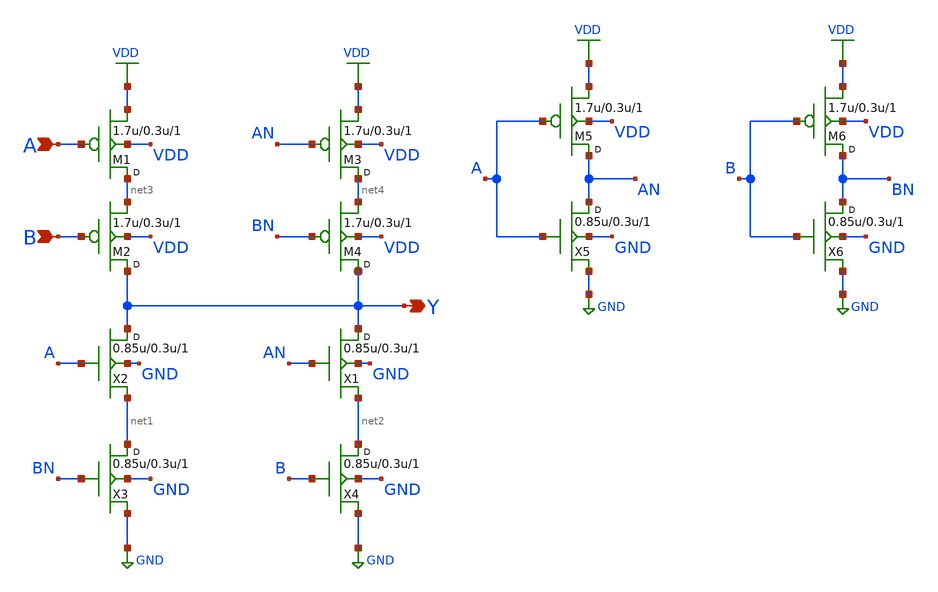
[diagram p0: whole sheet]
** sch_path: gf180mcu_osu_sc_gp12t3v3/cells/xnor2/gf180mcu_osu_sc_gp12t3v3__xnor2_1.sch
**.subckt gf180mcu_osu_sc_gp12t3v3__xnor2_1 B A Y
*.ipin B
*.ipin A
*.opin Y
X2 Y A net1 GND nfet_03p3 w=0.85u l=0.3u m=1
X3 net1 BN GND GND nfet_03p3 w=0.85u l=0.3u m=1
X1 Y AN net2 GND nfet_03p3 w=0.85u l=0.3u m=1
X4 net2 B GND GND nfet_03p3 w=0.85u l=0.3u m=1
M1 net3 A VDD VDD pfet_03p3 w=1.7u l=0.3u m=1
M2 Y B net3 VDD pfet_03p3 w=1.7u l=0.3u m=1
M3 net4 AN VDD VDD pfet_03p3 w=1.7u l=0.3u m=1
M4 Y BN net4 VDD pfet_03p3 w=1.7u l=0.3u m=1
X5 AN A GND GND nfet_03p3 w=0.85u l=0.3u m=1
M5 AN A VDD VDD pfet_03p3 w=1.7u l=0.3u m=1
X6 BN B GND GND nfet_03p3 w=0.85u l=0.3u m=1
M6 BN B VDD VDD pfet_03p3 w=1.7u l=0.3u m=1
**.ends
.GLOBAL GND
.GLOBAL VDD
.end
